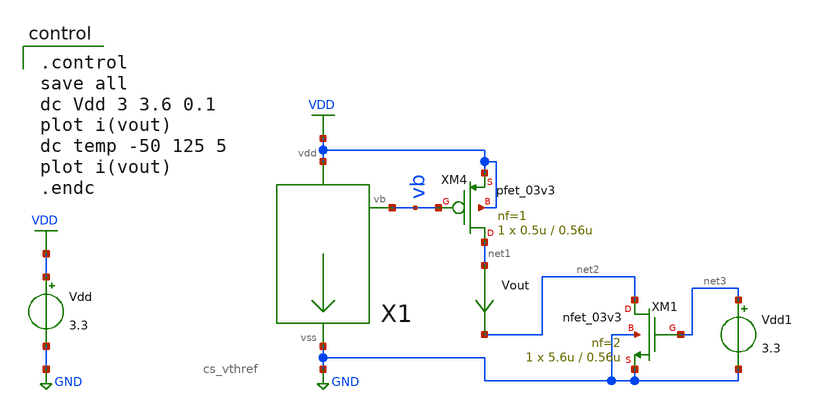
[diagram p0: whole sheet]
** sch_path: DAC/xschem/tb/tb_dc_cs_vthref.sch
**.subckt tb_dc_cs_vthref
Vdd VDD GND 3.3
X1 GND VDD vb cs_vthref
XM4 net1 vb VDD VDD pfet_03v3 L=0.56u W=0.5u nf=1 ad='int((nf+1)/2) * W/nf * 0.18u' as='int((nf+2)/2) * W/nf * 0.18u'
+ pd='2*int((nf+1)/2) * (W/nf + 0.18u)' ps='2*int((nf+2)/2) * (W/nf + 0.18u)' nrd='0.18u / W' nrs='0.18u / W'
+ sa=0 sb=0 sd=0 m=1
Vout net1 net2 0
.save i(vout)
XM1 net2 net3 GND GND nfet_03v3 L=0.56u W=5.6u nf=2 ad='int((nf+1)/2) * W/nf * 0.18u' as='int((nf+2)/2) * W/nf * 0.18u'
+ pd='2*int((nf+1)/2) * (W/nf + 0.18u)' ps='2*int((nf+2)/2) * (W/nf + 0.18u)' nrd='0.18u / W' nrs='0.18u / W'
+ sa=0 sb=0 sd=0 m=1
Vdd1 net3 GND 3.3
**** begin user architecture code

.include $::180MCU_MODELS/design.ngspice
.lib $::180MCU_MODELS/sm141064.ngspice typical
.lib $::180MCU_MODELS/sm141064.ngspice res_typical
.lib $::180MCU_MODELS/sm141064.ngspice moscap_typical
.lib $::180MCU_MODELS/sm141064.ngspice bjt_typical
* .lib $::180MCU_MODELS/sm141064.ngspice res_statistical


.control
save all
dc Vdd 3 3.6 0.1
plot i(vout)
dc temp -50 125 5
plot i(vout)
.endc

**** end user architecture code
**.ends
.GLOBAL GND
.GLOBAL VDD
.end
